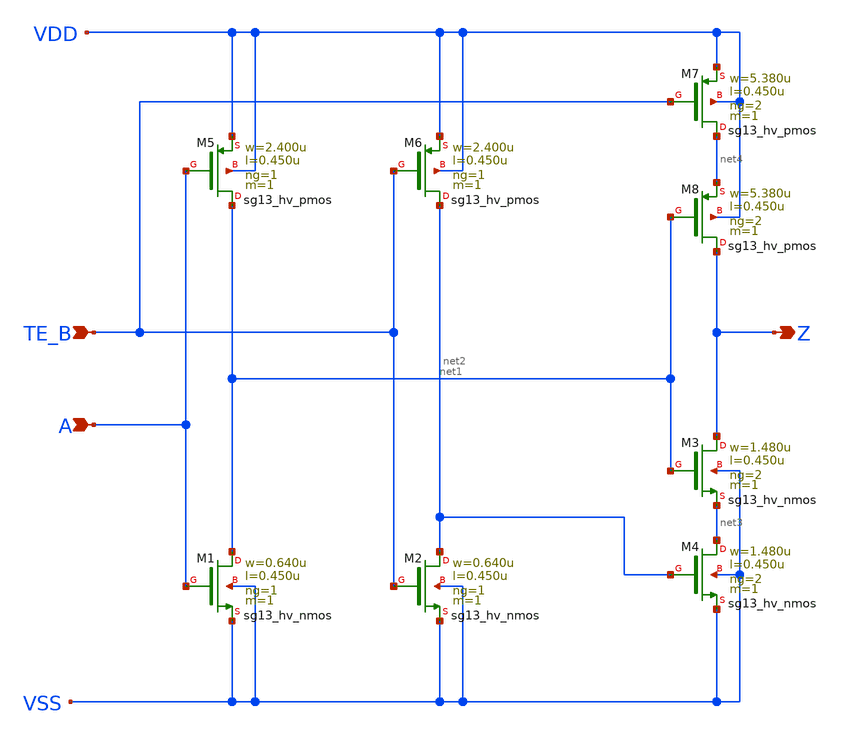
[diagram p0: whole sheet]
** sch_path: ihp-sg13g2/libs.ref/sg13g2_stdcell_hv/sch/xschem/sg13g2_hv_ebufn_2.sch
* Copyright 2023 IHP PDK Authors
* Licensed under the Apache License, Version 2.0 (the "License");
* you may not use this file except in compliance with the License.
* You may obtain a copy of the License at
* https://www.apache.org/licenses/LICENSE-2.0
* Unless required by applicable law or agreed to in writing, software
* distributed under the License is distributed on an "AS IS" BASIS,
* WITHOUT WARRANTIES OR CONDITIONS OF ANY KIND, either express or implied.
* See the License for the specific language governing permissions and
* limitations under the License.
**.subckt sg13g2_hv_ebufn_2 A TE_B Z
*.ipin A
*.ipin TE_B
*.opin Z
XM1 net1 A VSS VSS sg13_hv_nmos w=0.640u l=0.450u ng=1 m=1 mm_ok=1
XM2 net2 TE_B VSS VSS sg13_hv_nmos w=0.640u l=0.450u ng=1 m=1 mm_ok=1
XM3 Z net1 net3 VSS sg13_hv_nmos w=1.480u l=0.450u ng=2 m=1 mm_ok=1
XM4 net3 net2 VSS VSS sg13_hv_nmos w=1.480u l=0.450u ng=2 m=1 mm_ok=1
XM5 net1 A VDD VDD sg13_hv_pmos w=2.400u l=0.450u ng=1 m=1 mm_ok=1
XM6 net2 TE_B VDD VDD sg13_hv_pmos w=2.400u l=0.450u ng=1 m=1 mm_ok=1
XM7 net4 TE_B VDD VDD sg13_hv_pmos w=5.380u l=0.450u ng=2 m=1 mm_ok=1
XM8 Z net1 net4 VDD sg13_hv_pmos w=5.380u l=0.450u ng=2 m=1 mm_ok=1
**.ends
.end
